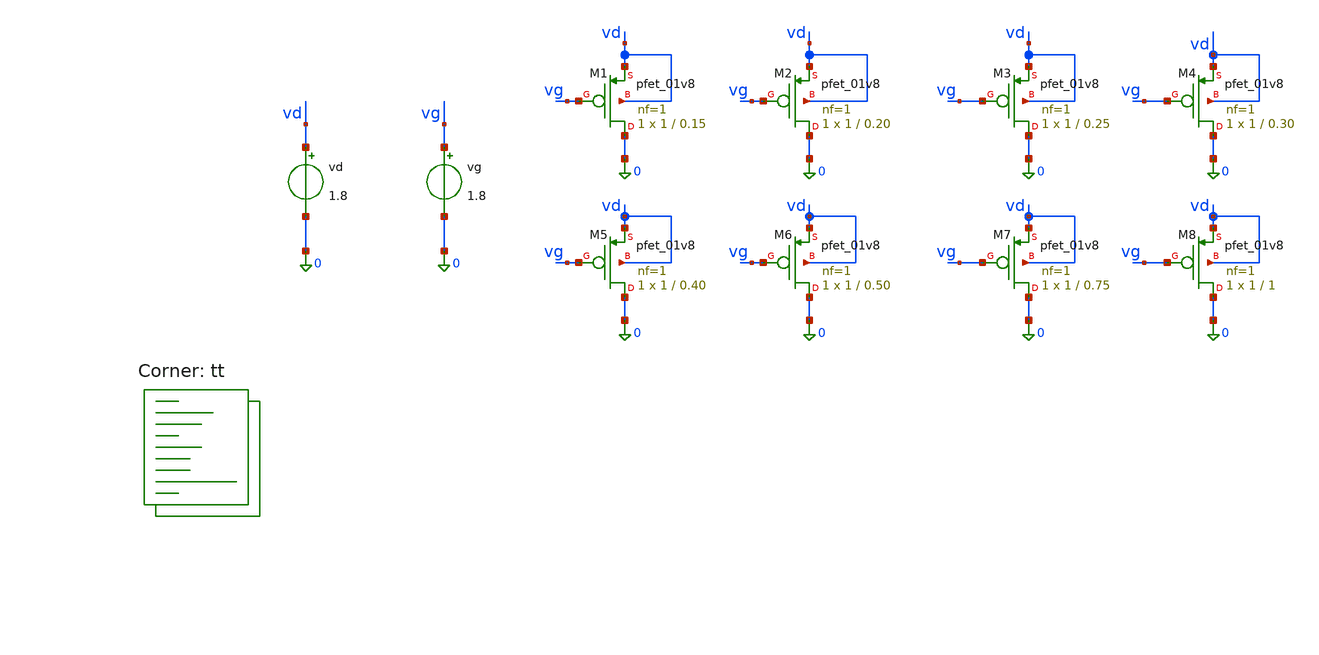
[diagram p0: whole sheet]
** sch_path: Gm_ID (SKY 130) of BGR/gmidpmossky.sch
**.subckt gmidpmossky
vd vd 0 1.8
vg vg 0 1.8
XM1 0 vg vd vd sky130_fd_pr__pfet_01v8 L=0.15 W=1 nf=1 ad='int((1 + 1)/2) * 1 / 1 * 0.29' as='int((1 + 2)/2) * 1 / 1 * 0.29'
+ pd='2*int((1 + 1)/2) * (1 / 1 + 0.29)' ps='2*int((1 + 2)/2) * (1 / 1 + 0.29)' nrd='0.29 / 1 ' nrs='0.29 / 1 '
+ sa=0 sb=0 sd=0 mult=1 m=1
XM2 0 vg vd vd sky130_fd_pr__pfet_01v8 L=0.20 W=1 nf=1 ad='int((1 + 1)/2) * 1 / 1 * 0.29' as='int((1 + 2)/2) * 1 / 1 * 0.29'
+ pd='2*int((1 + 1)/2) * (1 / 1 + 0.29)' ps='2*int((1 + 2)/2) * (1 / 1 + 0.29)' nrd='0.29 / 1 ' nrs='0.29 / 1 '
+ sa=0 sb=0 sd=0 mult=1 m=1
XM3 0 vg vd vd sky130_fd_pr__pfet_01v8 L=0.25 W=1 nf=1 ad='int((1 + 1)/2) * 1 / 1 * 0.29' as='int((1 + 2)/2) * 1 / 1 * 0.29'
+ pd='2*int((1 + 1)/2) * (1 / 1 + 0.29)' ps='2*int((1 + 2)/2) * (1 / 1 + 0.29)' nrd='0.29 / 1 ' nrs='0.29 / 1 '
+ sa=0 sb=0 sd=0 mult=1 m=1
XM4 0 vg vd vd sky130_fd_pr__pfet_01v8 L=0.30 W=1 nf=1 ad='int((1 + 1)/2) * 1 / 1 * 0.29' as='int((1 + 2)/2) * 1 / 1 * 0.29'
+ pd='2*int((1 + 1)/2) * (1 / 1 + 0.29)' ps='2*int((1 + 2)/2) * (1 / 1 + 0.29)' nrd='0.29 / 1 ' nrs='0.29 / 1 '
+ sa=0 sb=0 sd=0 mult=1 m=1
XM5 0 vg vd vd sky130_fd_pr__pfet_01v8 L=0.40 W=1 nf=1 ad='int((1 + 1)/2) * 1 / 1 * 0.29' as='int((1 + 2)/2) * 1 / 1 * 0.29'
+ pd='2*int((1 + 1)/2) * (1 / 1 + 0.29)' ps='2*int((1 + 2)/2) * (1 / 1 + 0.29)' nrd='0.29 / 1 ' nrs='0.29 / 1 '
+ sa=0 sb=0 sd=0 mult=1 m=1
XM6 0 vg vd vd sky130_fd_pr__pfet_01v8 L=0.50 W=1 nf=1 ad='int((1 + 1)/2) * 1 / 1 * 0.29' as='int((1 + 2)/2) * 1 / 1 * 0.29'
+ pd='2*int((1 + 1)/2) * (1 / 1 + 0.29)' ps='2*int((1 + 2)/2) * (1 / 1 + 0.29)' nrd='0.29 / 1 ' nrs='0.29 / 1 '
+ sa=0 sb=0 sd=0 mult=1 m=1
XM7 0 vg vd vd sky130_fd_pr__pfet_01v8 L=0.75 W=1 nf=1 ad='int((1 + 1)/2) * 1 / 1 * 0.29' as='int((1 + 2)/2) * 1 / 1 * 0.29'
+ pd='2*int((1 + 1)/2) * (1 / 1 + 0.29)' ps='2*int((1 + 2)/2) * (1 / 1 + 0.29)' nrd='0.29 / 1 ' nrs='0.29 / 1 '
+ sa=0 sb=0 sd=0 mult=1 m=1
XM8 0 vg vd vd sky130_fd_pr__pfet_01v8 L=1 W=1 nf=1 ad='int((1 + 1)/2) * 1 / 1 * 0.29' as='int((1 + 2)/2) * 1 / 1 * 0.29'
+ pd='2*int((1 + 1)/2) * (1 / 1 + 0.29)' ps='2*int((1 + 2)/2) * (1 / 1 + 0.29)' nrd='0.29 / 1 ' nrs='0.29 / 1 '
+ sa=0 sb=0 sd=0 mult=1 m=1
**** begin user architecture code

** opencircuitdesign pdks install
.lib $::SKYWATER_MODELS/sky130.lib.spice tt

.lib $::SKYWATER_MODELS/sky130.lib.spice tt


.option wnflag=1
.option savecurrents

.control



*M1
save @m.xm1.msky130_fd_pr__pfet_01v8[gm]
save @m.xm1.msky130_fd_pr__pfet_01v8[id]
save @m.xm1.msky130_fd_pr__pfet_01v8[vgs]
save @m.xm1.msky130_fd_pr__pfet_01v8[gds]
save @m.xm1.msky130_fd_pr__pfet_01v8[cgg]
save @m.xm1.msky130_fd_pr__pfet_01v8[vds]
save @m.xm1.msky130_fd_pr__pfet_01v8[vth]

*M2
save @m.xm2.msky130_fd_pr__pfet_01v8[gm]
save @m.xm2.msky130_fd_pr__pfet_01v8[id]
save @m.xm2.msky130_fd_pr__pfet_01v8[vgs]
save @m.xm2.msky130_fd_pr__pfet_01v8[gds]
save @m.xm2.msky130_fd_pr__pfet_01v8[cgg]
save @m.xm2.msky130_fd_pr__pfet_01v8[vds]
save @m.xm2.msky130_fd_pr__pfet_01v8[vth]

*M3
save @m.xm3.msky130_fd_pr__pfet_01v8[gm]
save @m.xm3.msky130_fd_pr__pfet_01v8[id]
save @m.xm3.msky130_fd_pr__pfet_01v8[vgs]
save @m.xm3.msky130_fd_pr__pfet_01v8[gds]
save @m.xm3.msky130_fd_pr__pfet_01v8[cgg]
save @m.xm3.msky130_fd_pr__pfet_01v8[vds]
save @m.xm3.msky130_fd_pr__pfet_01v8[vth]

*M4
save @m.xm4.msky130_fd_pr__pfet_01v8[gm]
save @m.xm4.msky130_fd_pr__pfet_01v8[id]
save @m.xm4.msky130_fd_pr__pfet_01v8[vgs]
save @m.xm4.msky130_fd_pr__pfet_01v8[gds]
save @m.xm4.msky130_fd_pr__pfet_01v8[cgg]
save @m.xm4.msky130_fd_pr__pfet_01v8[vds]
save @m.xm4.msky130_fd_pr__pfet_01v8[vth]


*M5
save @m.xm5.msky130_fd_pr__pfet_01v8[gm]
save @m.xm5.msky130_fd_pr__pfet_01v8[id]
save @m.xm5.msky130_fd_pr__pfet_01v8[vgs]
save @m.xm5.msky130_fd_pr__pfet_01v8[gds]
save @m.xm5.msky130_fd_pr__pfet_01v8[cgg]
save @m.xm5.msky130_fd_pr__pfet_01v8[vds]
save @m.xm5.msky130_fd_pr__pfet_01v8[vth]

*M6
save @m.xm6.msky130_fd_pr__pfet_01v8[gm]
save @m.xm6.msky130_fd_pr__pfet_01v8[id]
save @m.xm6.msky130_fd_pr__pfet_01v8[vgs]
save @m.xm6.msky130_fd_pr__pfet_01v8[gds]
save @m.xm6.msky130_fd_pr__pfet_01v8[cgg]
save @m.xm6.msky130_fd_pr__pfet_01v8[vds]
save @m.xm6.msky130_fd_pr__pfet_01v8[vth]

*M7
save @m.xm7.msky130_fd_pr__pfet_01v8[gm]
save @m.xm7.msky130_fd_pr__pfet_01v8[id]
save @m.xm7.msky130_fd_pr__pfet_01v8[vgs]
save @m.xm7.msky130_fd_pr__pfet_01v8[gds]
save @m.xm7.msky130_fd_pr__pfet_01v8[cgg]
save @m.xm7.msky130_fd_pr__pfet_01v8[vds]
save @m.xm7.msky130_fd_pr__pfet_01v8[vth]

*M8
save @m.xm8.msky130_fd_pr__pfet_01v8[gm]
save @m.xm8.msky130_fd_pr__pfet_01v8[id]
save @m.xm8.msky130_fd_pr__pfet_01v8[vgs]
save @m.xm8.msky130_fd_pr__pfet_01v8[gds]
save @m.xm8.msky130_fd_pr__pfet_01v8[cgg]
save @m.xm8.msky130_fd_pr__pfet_01v8[vds]
save @m.xm8.msky130_fd_pr__pfet_01v8[vth]


remzerovec
dc vg 0.05 1.8 0.01

write sky130_pmos.raw

wrdata sky130_pmos1.txt  @m.xm1.msky130_fd_pr__pfet_01v8[gm]  @m.xm1.msky130_fd_pr__pfet_01v8[id]
+  @m.xm1.msky130_fd_pr__pfet_01v8[vgs]  @m.xm1.msky130_fd_pr__pfet_01v8[gds]  @m.xm1.msky130_fd_pr__pfet_01v8[cgg]
+  @m.xm1.msky130_fd_pr__pfet_01v8[vds]  @m.xm1.msky130_fd_pr__pfet_01v8[vth]

wrdata sky130_pmos2.txt  @m.xm2.msky130_fd_pr__pfet_01v8[gm]  @m.xm2.msky130_fd_pr__pfet_01v8[id]
+  @m.xm2.msky130_fd_pr__pfet_01v8[vgs]  @m.xm2.msky130_fd_pr__pfet_01v8[gds]  @m.xm2.msky130_fd_pr__pfet_01v8[cgg]
+  @m.xm2.msky130_fd_pr__pfet_01v8[vds]  @m.xm2.msky130_fd_pr__pfet_01v8[vth]

wrdata sky130_pmos3.txt  @m.xm3.msky130_fd_pr__pfet_01v8[gm]  @m.xm3.msky130_fd_pr__pfet_01v8[id]
+  @m.xm3.msky130_fd_pr__pfet_01v8[vgs]  @m.xm3.msky130_fd_pr__pfet_01v8[gds]  @m.xm3.msky130_fd_pr__pfet_01v8[cgg]
+  @m.xm3.msky130_fd_pr__pfet_01v8[vds]  @m.xm3.msky130_fd_pr__pfet_01v8[vth]

wrdata sky130_pmos4.txt  @m.xm4.msky130_fd_pr__pfet_01v8[gm]  @m.xm4.msky130_fd_pr__pfet_01v8[id]
+  @m.xm4.msky130_fd_pr__pfet_01v8[vgs]  @m.xm4.msky130_fd_pr__pfet_01v8[gds]  @m.xm4.msky130_fd_pr__pfet_01v8[cgg]
+  @m.xm4.msky130_fd_pr__pfet_01v8[vds]  @m.xm4.msky130_fd_pr__pfet_01v8[vth]

wrdata sky130_pmos5.txt  @m.xm5.msky130_fd_pr__pfet_01v8[gm]  @m.xm5.msky130_fd_pr__pfet_01v8[id]
+  @m.xm5.msky130_fd_pr__pfet_01v8[vgs]  @m.xm5.msky130_fd_pr__pfet_01v8[gds]  @m.xm5.msky130_fd_pr__pfet_01v8[cgg]
+  @m.xm5.msky130_fd_pr__pfet_01v8[vds]  @m.xm5.msky130_fd_pr__pfet_01v8[vth]

wrdata sky130_pmos6.txt  @m.xm6.msky130_fd_pr__pfet_01v8[gm]  @m.xm6.msky130_fd_pr__pfet_01v8[id]
+  @m.xm6.msky130_fd_pr__pfet_01v8[vgs]  @m.xm6.msky130_fd_pr__pfet_01v8[gds]  @m.xm6.msky130_fd_pr__pfet_01v8[cgg]
+  @m.xm6.msky130_fd_pr__pfet_01v8[vds]  @m.xm6.msky130_fd_pr__pfet_01v8[vth]

wrdata sky130_pmos7.txt  @m.xm7.msky130_fd_pr__pfet_01v8[gm]  @m.xm7.msky130_fd_pr__pfet_01v8[id]
+  @m.xm7.msky130_fd_pr__pfet_01v8[vgs]  @m.xm7.msky130_fd_pr__pfet_01v8[gds]  @m.xm7.msky130_fd_pr__pfet_01v8[cgg]
+  @m.xm7.msky130_fd_pr__pfet_01v8[vds]  @m.xm7.msky130_fd_pr__pfet_01v8[vth]

wrdata sky130_pmos8.txt  @m.xm8.msky130_fd_pr__pfet_01v8[gm]  @m.xm8.msky130_fd_pr__pfet_01v8[id]
+  @m.xm8.msky130_fd_pr__pfet_01v8[vgs]  @m.xm8.msky130_fd_pr__pfet_01v8[gds]  @m.xm8.msky130_fd_pr__pfet_01v8[cgg]
+  @m.xm8.msky130_fd_pr__pfet_01v8[vds]  @m.xm8.msky130_fd_pr__pfet_01v8[vth]


let gmid1= @m.xm1.msky130_fd_pr__pfet_01v8[gm]/abs(@m.xm1.msky130_fd_pr__pfet_01v8[id])
let gmid2= @m.xm2.msky130_fd_pr__pfet_01v8[gm]/abs(@m.xm2.msky130_fd_pr__pfet_01v8[id])
let gmid3= @m.xm3.msky130_fd_pr__pfet_01v8[gm]/abs(@m.xm3.msky130_fd_pr__pfet_01v8[id])
let gmid4= @m.xm4.msky130_fd_pr__pfet_01v8[gm]/abs(@m.xm4.msky130_fd_pr__pfet_01v8[id])
let gmid5= @m.xm5.msky130_fd_pr__pfet_01v8[gm]/abs(@m.xm5.msky130_fd_pr__pfet_01v8[id])
let gmid6= @m.xm6.msky130_fd_pr__pfet_01v8[gm]/abs(@m.xm6.msky130_fd_pr__pfet_01v8[id])
let gmid7= @m.xm7.msky130_fd_pr__pfet_01v8[gm]/abs(@m.xm7.msky130_fd_pr__pfet_01v8[id])
let gmid8= @m.xm8.msky130_fd_pr__pfet_01v8[gm]/abs(@m.xm8.msky130_fd_pr__pfet_01v8[id])

let vov1= abs(@m.xm1.msky130_fd_pr__pfet_01v8[vgs])-abs(@m.xm1.msky130_fd_pr__pfet_01v8[vth])
let vov2= abs(@m.xm2.msky130_fd_pr__pfet_01v8[vgs])-abs(@m.xm2.msky130_fd_pr__pfet_01v8[vth])
let vov3= abs(@m.xm3.msky130_fd_pr__pfet_01v8[vgs])-abs(@m.xm3.msky130_fd_pr__pfet_01v8[vth])
let vov4= abs(@m.xm4.msky130_fd_pr__pfet_01v8[vgs])-abs(@m.xm4.msky130_fd_pr__pfet_01v8[vth])
let vov5= abs(@m.xm5.msky130_fd_pr__pfet_01v8[vgs])-abs(@m.xm5.msky130_fd_pr__pfet_01v8[vth])
let vov6= abs(@m.xm6.msky130_fd_pr__pfet_01v8[vgs])-abs(@m.xm6.msky130_fd_pr__pfet_01v8[vth])
let vov7= abs(@m.xm7.msky130_fd_pr__pfet_01v8[vgs])-abs(@m.xm7.msky130_fd_pr__pfet_01v8[vth])
let vov8= abs(@m.xm8.msky130_fd_pr__pfet_01v8[vgs])-abs(@m.xm8.msky130_fd_pr__pfet_01v8[vth])

let gmgds1= @m.xm1.msky130_fd_pr__pfet_01v8[gm]/@m.xm1.msky130_fd_pr__pfet_01v8[gds]
let gmgds2= @m.xm2.msky130_fd_pr__pfet_01v8[gm]/@m.xm2.msky130_fd_pr__pfet_01v8[gds]
let gmgds3= @m.xm3.msky130_fd_pr__pfet_01v8[gm]/@m.xm3.msky130_fd_pr__pfet_01v8[gds]
let gmgds4= @m.xm4.msky130_fd_pr__pfet_01v8[gm]/@m.xm4.msky130_fd_pr__pfet_01v8[gds]
let gmgds5= @m.xm5.msky130_fd_pr__pfet_01v8[gm]/@m.xm5.msky130_fd_pr__pfet_01v8[gds]
let gmgds6= @m.xm6.msky130_fd_pr__pfet_01v8[gm]/@m.xm6.msky130_fd_pr__pfet_01v8[gds]
let gmgds7= @m.xm7.msky130_fd_pr__pfet_01v8[gm]/@m.xm7.msky130_fd_pr__pfet_01v8[gds]
let gmgds8= @m.xm8.msky130_fd_pr__pfet_01v8[gm]/@m.xm8.msky130_fd_pr__pfet_01v8[gds]

let w = 1u

let ft1=@m.xm1.msky130_fd_pr__pfet_01v8[gm]/(2*3.14*@m.xm1.msky130_fd_pr__pfet_01v8[cgg])
let ft2=@m.xm2.msky130_fd_pr__pfet_01v8[gm]/(2*3.14*@m.xm2.msky130_fd_pr__pfet_01v8[cgg])
let ft3=@m.xm3.msky130_fd_pr__pfet_01v8[gm]/(2*3.14*@m.xm3.msky130_fd_pr__pfet_01v8[cgg])
let ft4=@m.xm4.msky130_fd_pr__pfet_01v8[gm]/(2*3.14*@m.xm4.msky130_fd_pr__pfet_01v8[cgg])
let ft5=@m.xm5.msky130_fd_pr__pfet_01v8[gm]/(2*3.14*@m.xm5.msky130_fd_pr__pfet_01v8[cgg])
let ft6=@m.xm6.msky130_fd_pr__pfet_01v8[gm]/(2*3.14*@m.xm6.msky130_fd_pr__pfet_01v8[cgg])
let ft7=@m.xm7.msky130_fd_pr__pfet_01v8[gm]/(2*3.14*@m.xm7.msky130_fd_pr__pfet_01v8[cgg])
let ft8=@m.xm8.msky130_fd_pr__pfet_01v8[gm]/(2*3.14*@m.xm8.msky130_fd_pr__pfet_01v8[cgg])

let idw1=@m.xm1.msky130_fd_pr__pfet_01v8[id]/w
let idw2=@m.xm2.msky130_fd_pr__pfet_01v8[id]/w
let idw3=@m.xm3.msky130_fd_pr__pfet_01v8[id]/w
let idw4=@m.xm4.msky130_fd_pr__pfet_01v8[id]/w
let idw5=@m.xm5.msky130_fd_pr__pfet_01v8[id]/w
let idw6=@m.xm6.msky130_fd_pr__pfet_01v8[id]/w
let idw7=@m.xm7.msky130_fd_pr__pfet_01v8[id]/w
let idw8=@m.xm8.msky130_fd_pr__pfet_01v8[id]/w




set appendwrite
remzerovec
.endc


**** end user architecture code
**.ends
.end
